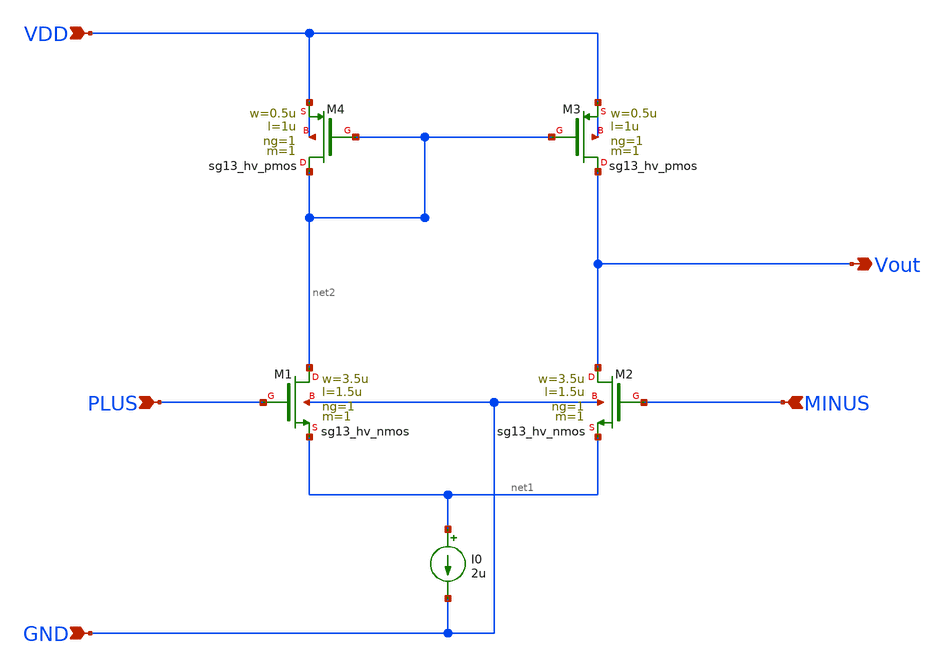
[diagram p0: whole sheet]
** sch_path: Design Files/RAMP/OTA/NOTA2.sch
**.subckt NOTA2 VDD GND PLUS MINUS Vout
*.ipin VDD
*.ipin GND
*.ipin PLUS
*.ipin MINUS
*.opin Vout
XM1 net2 PLUS net1 GND sg13_hv_nmos w=3.5u l=1.5u ng=1 m=1 mm_ok=1
XM2 Vout MINUS net1 GND sg13_hv_nmos w=3.5u l=1.5u ng=1 m=1 mm_ok=1
I0 net1 GND 2u
XM3 Vout net2 VDD VDD sg13_hv_pmos w=0.5u l=1u ng=1 m=1 mm_ok=1
XM4 net2 net2 VDD VDD sg13_hv_pmos w=0.5u l=1u ng=1 m=1 mm_ok=1
**.ends
.end
